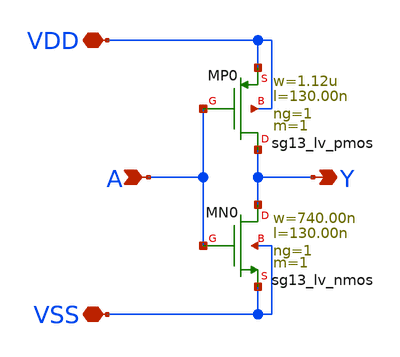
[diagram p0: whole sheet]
** sch_path: ihp-sg13cmos5l/libs.tech/xschem/sg13cmos5l_stdcells/sg13cmos5l_inv_1.sch
* Copyright 2025 IHP PDK Authors
* Licensed under the Apache License, Version 2.0 (the "License");
* you may not use this file except in compliance with the License.
* You may obtain a copy of the License at
* https://www.apache.org/licenses/LICENSE-2.0
* Unless required by applicable law or agreed to in writing, software
* distributed under the License is distributed on an "AS IS" BASIS,
* WITHOUT WARRANTIES OR CONDITIONS OF ANY KIND, either express or implied.
* See the License for the specific language governing permissions and
* limitations under the License.
**.subckt sg13cmos5l_inv_1 Y A VDD VSS
*.opin Y
*.ipin A
*.iopin VDD
*.iopin VSS
XMN0 Y A VSS VSS sg13_lv_nmos w=740.00n l=130.00n ng=1 m=1 mm_ok=1
XMP0 Y A VDD VDD sg13_lv_pmos w=1.12u l=130.00n ng=1 m=1 mm_ok=1
**.ends
.end
